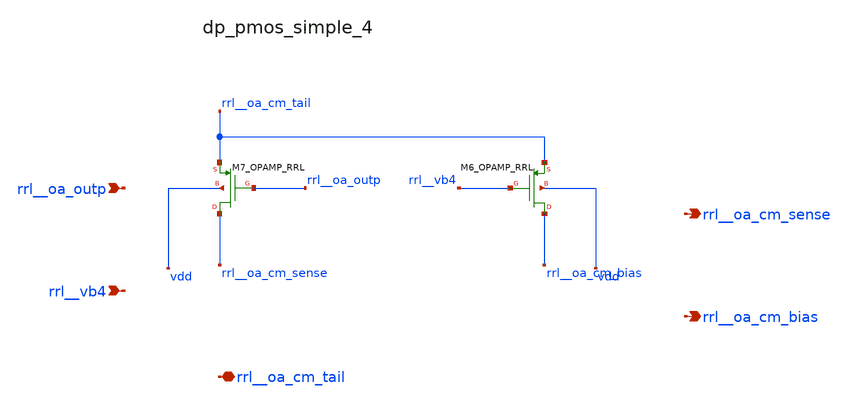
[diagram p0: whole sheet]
** sch_path: analog-db/raw/ia_004_fan_chopper_rrl/hier/blocks/dp_pmos_simple_4.sch
**.subckt dp_pmos_simple_4 rrl__oa_outp rrl__vb4 rrl__oa_cm_tail rrl__oa_cm_sense rrl__oa_cm_bias
*.ipin rrl__oa_outp
*.ipin rrl__vb4
*.iopin rrl__oa_cm_tail
*.opin rrl__oa_cm_sense
*.opin rrl__oa_cm_bias
XM6_OPAMP_RRL rrl__oa_cm_bias rrl__vb4 rrl__oa_cm_tail vdd sg13_lv_pmos w=x_dut_xm6_opamp_rrl_w
+ l=x_dut_xm6_opamp_rrl_l ng=1 m=x_dut_xm6_opamp_rrl_m
XM7_OPAMP_RRL rrl__oa_cm_sense rrl__oa_outp rrl__oa_cm_tail vdd sg13_lv_pmos w=x_dut_xm7_opamp_rrl_w
+ l=x_dut_xm7_opamp_rrl_l ng=1 m=x_dut_xm7_opamp_rrl_m
**.ends
.end
